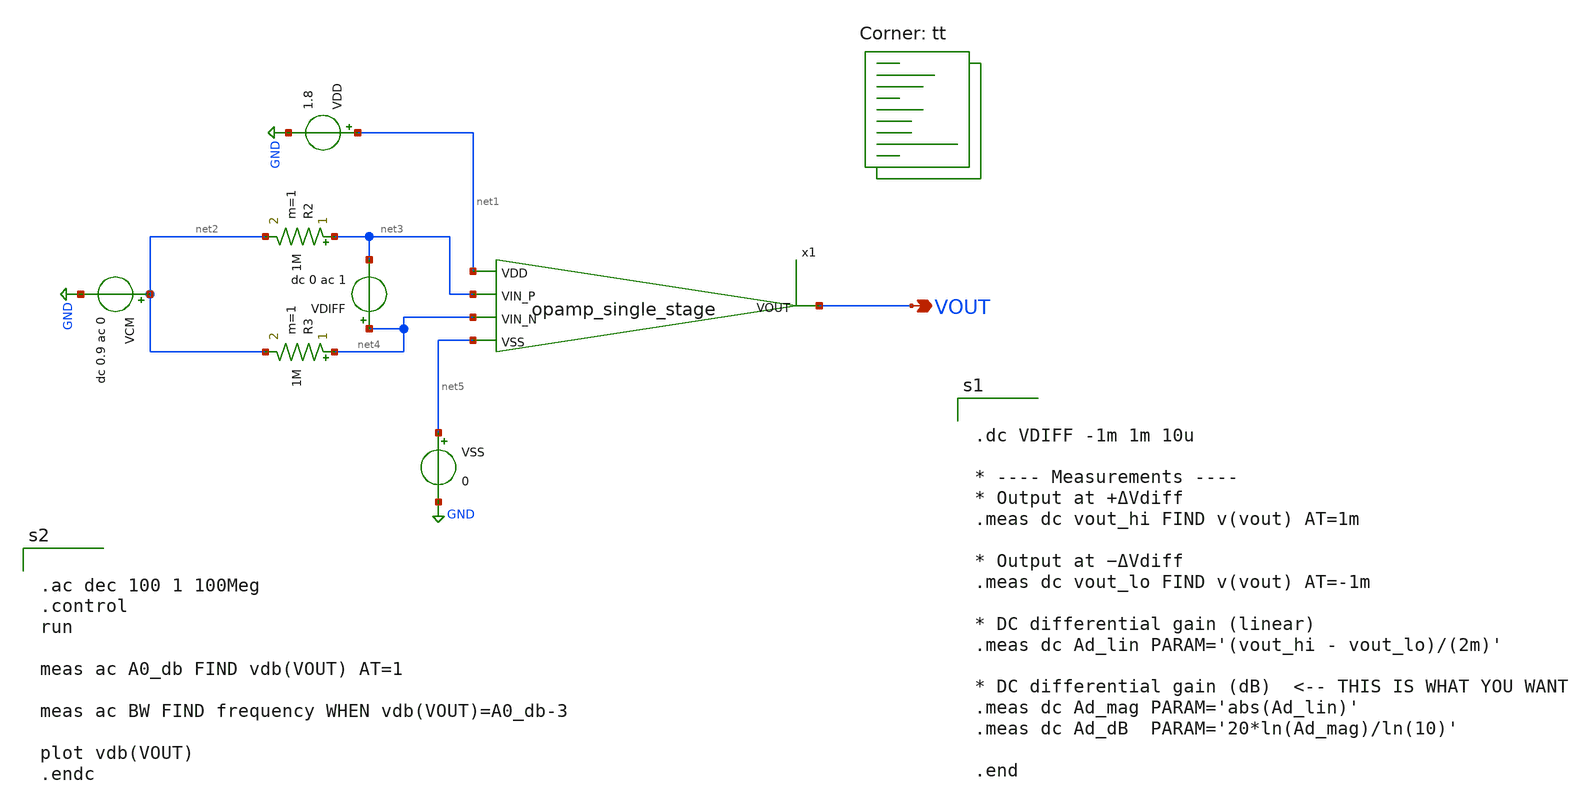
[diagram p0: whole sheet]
** sch_path: analog/schematics/testbenches/tb_ac_analysis.sch
**.subckt tb_ac_analysis VOUT
*.opin VOUT
VDD net1 GND 1.8
VSS net5 GND 0
VCM net2 GND dc 0.9 ac 0
R2 net3 net2 1M m=1
R3 net4 net2 1M m=1
VDIFF net4 net3 dc 0 ac 1
x1 net1 VOUT net3 net4 net5 opamp_single_stage
**** begin user architecture code
.lib $::SKYWATER_MODELS/sky130.lib.spice tt


.dc VDIFF -1m 1m 10u

* ---- Measurements ----
* Output at +ΔVdiff
.meas dc vout_hi FIND v(vout) AT=1m

* Output at −ΔVdiff
.meas dc vout_lo FIND v(vout) AT=-1m

* DC differential gain (linear)
.meas dc Ad_lin PARAM='(vout_hi - vout_lo)/(2m)'

* DC differential gain (dB)  <-- THIS IS WHAT YOU WANT
.meas dc Ad_mag PARAM='abs(Ad_lin)'
.meas dc Ad_dB  PARAM='20*ln(Ad_mag)/ln(10)'

.end




.ac dec 100 1 100Meg
.control
run

meas ac A0_db FIND vdb(VOUT) AT=1

meas ac BW FIND frequency WHEN vdb(VOUT)=A0_db-3

plot vdb(VOUT)
.endc


**** end user architecture code
**.ends

* expanding   symbol:  opamp_single_stage.sym # of pins=5
** sym_path: analog/schematics/opamp_single_stage.sym
** sch_path: analog/schematics/opamp_single_stage.sch
.subckt opamp_single_stage VDD VOUT VIN_P VIN_N VSS
*.ipin VDD
*.ipin VIN_P
*.ipin VIN_N
*.ipin VSS
*.opin VOUT
XM4 net2 net1 VDD VDD sky130_fd_pr__pfet_01v8 L=0.5 W=8 nf=1 ad='int((nf+1)/2) * W/nf * 0.29' as='int((nf+2)/2) * W/nf * 0.29'
+ pd='2*int((nf+1)/2) * (W/nf + 0.29)' ps='2*int((nf+2)/2) * (W/nf + 0.29)' nrd='0.29 / W' nrs='0.29 / W'
+ sa=0 sb=0 sd=0 mult=1 m=1
XM3 net1 net1 VDD VDD sky130_fd_pr__pfet_01v8 L=0.5 W=8 nf=1 ad='int((nf+1)/2) * W/nf * 0.29' as='int((nf+2)/2) * W/nf * 0.29'
+ pd='2*int((nf+1)/2) * (W/nf + 0.29)' ps='2*int((nf+2)/2) * (W/nf + 0.29)' nrd='0.29 / W' nrs='0.29 / W'
+ sa=0 sb=0 sd=0 mult=1 m=1
XM1 net1 VIN_P net3 GND sky130_fd_pr__nfet_01v8_lvt L=0.5 W=6 nf=1 ad='int((nf+1)/2) * W/nf * 0.29' as='int((nf+2)/2) * W/nf * 0.29'
+ pd='2*int((nf+1)/2) * (W/nf + 0.29)' ps='2*int((nf+2)/2) * (W/nf + 0.29)' nrd='0.29 / W' nrs='0.29 / W'
+ sa=0 sb=0 sd=0 mult=1 m=1
XM2 net2 VIN_N net3 GND sky130_fd_pr__nfet_01v8_lvt L=0.5 W=6 nf=1 ad='int((nf+1)/2) * W/nf * 0.29' as='int((nf+2)/2) * W/nf * 0.29'
+ pd='2*int((nf+1)/2) * (W/nf + 0.29)' ps='2*int((nf+2)/2) * (W/nf + 0.29)' nrd='0.29 / W' nrs='0.29 / W'
+ sa=0 sb=0 sd=0 mult=1 m=1
XM5 VOUT net2 VDD VDD sky130_fd_pr__pfet_01v8 L=0.5 W=20 nf=1 ad='int((nf+1)/2) * W/nf * 0.29' as='int((nf+2)/2) * W/nf * 0.29'
+ pd='2*int((nf+1)/2) * (W/nf + 0.29)' ps='2*int((nf+2)/2) * (W/nf + 0.29)' nrd='0.29 / W' nrs='0.29 / W'
+ sa=0 sb=0 sd=0 mult=1 m=1
XC1 net5 VOUT sky130_fd_pr__cap_mim_m3_1 W=25 L=20 MF=1 m=1
XM8 net4 net4 VSS VSS sky130_fd_pr__nfet_01v8_lvt L=1.0 W=2 nf=1 ad='int((nf+1)/2) * W/nf * 0.29' as='int((nf+2)/2) * W/nf * 0.29'
+ pd='2*int((nf+1)/2) * (W/nf + 0.29)' ps='2*int((nf+2)/2) * (W/nf + 0.29)' nrd='0.29 / W' nrs='0.29 / W'
+ sa=0 sb=0 sd=0 mult=1 m=1
XM7 net3 net4 VSS VSS sky130_fd_pr__nfet_01v8_lvt L=1.0 W=4 nf=1 ad='int((nf+1)/2) * W/nf * 0.29' as='int((nf+2)/2) * W/nf * 0.29'
+ pd='2*int((nf+1)/2) * (W/nf + 0.29)' ps='2*int((nf+2)/2) * (W/nf + 0.29)' nrd='0.29 / W' nrs='0.29 / W'
+ sa=0 sb=0 sd=0 mult=1 m=1
XM6 VOUT net4 VSS VSS sky130_fd_pr__nfet_01v8_lvt L=1.0 W=8 nf=1 ad='int((nf+1)/2) * W/nf * 0.29' as='int((nf+2)/2) * W/nf * 0.29'
+ pd='2*int((nf+1)/2) * (W/nf + 0.29)' ps='2*int((nf+2)/2) * (W/nf + 0.29)' nrd='0.29 / W' nrs='0.29 / W'
+ sa=0 sb=0 sd=0 mult=1 m=1
I0 VDD net4 5u
R1 net5 net2 7k m=1
.ends

.GLOBAL GND
.end
